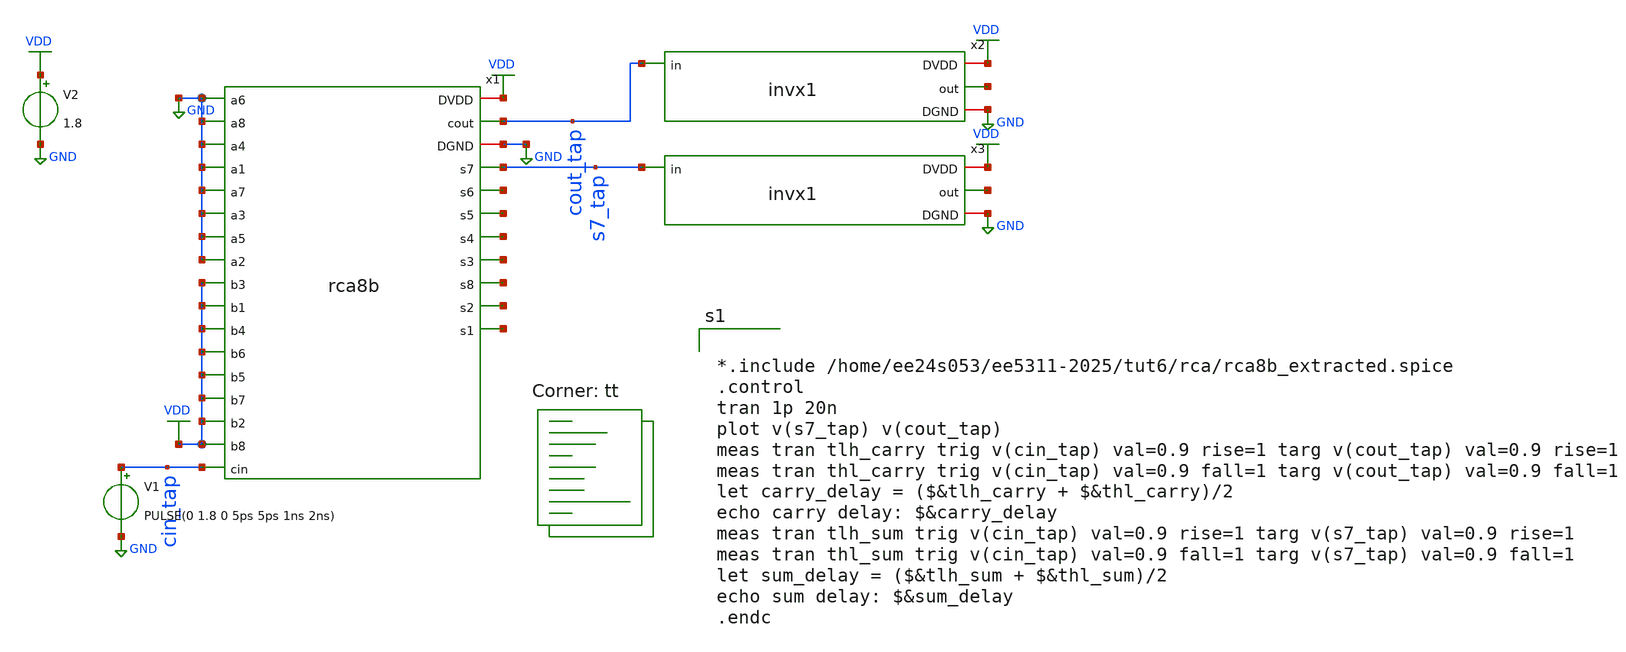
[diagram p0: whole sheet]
** sch_path: tut6/rca/rca8b_tb.sch
**.subckt rca8b_tb
x1 GND GND GND GND GND GND GND GND VDD VDD VDD VDD VDD VDD VDD VDD VDD cout_tap cin_tap GND s7_tap
+ net1 net2 net3 net4 net5 net6 net7 rca8b
V1 cin_tap GND PULSE(0 1.8 0 5ps 5ps 1ns 2ns)
V2 VDD GND 1.8
x2 VDD cout_tap net8 GND invx1
x3 VDD s7_tap net9 GND invx1
**** begin user architecture code
.lib $::SKYWATER_MODELS/sky130.lib.spice tt


*.include /home/ee24s053/ee5311-2025/tut6/rca/rca8b_extracted.spice
.control
tran 1p 20n
plot v(s7_tap) v(cout_tap)
meas tran tlh_carry trig v(cin_tap) val=0.9 rise=1 targ v(cout_tap) val=0.9 rise=1
meas tran thl_carry trig v(cin_tap) val=0.9 fall=1 targ v(cout_tap) val=0.9 fall=1
let carry_delay = ($&tlh_carry + $&thl_carry)/2
echo carry delay: $&carry_delay
meas tran tlh_sum trig v(cin_tap) val=0.9 rise=1 targ v(s7_tap) val=0.9 rise=1
meas tran thl_sum trig v(cin_tap) val=0.9 fall=1 targ v(s7_tap) val=0.9 fall=1
let sum_delay = ($&tlh_sum + $&thl_sum)/2
echo sum delay: $&sum_delay
.endc

**** end user architecture code
**.ends
.GLOBAL VDD
.GLOBAL GND
.end
